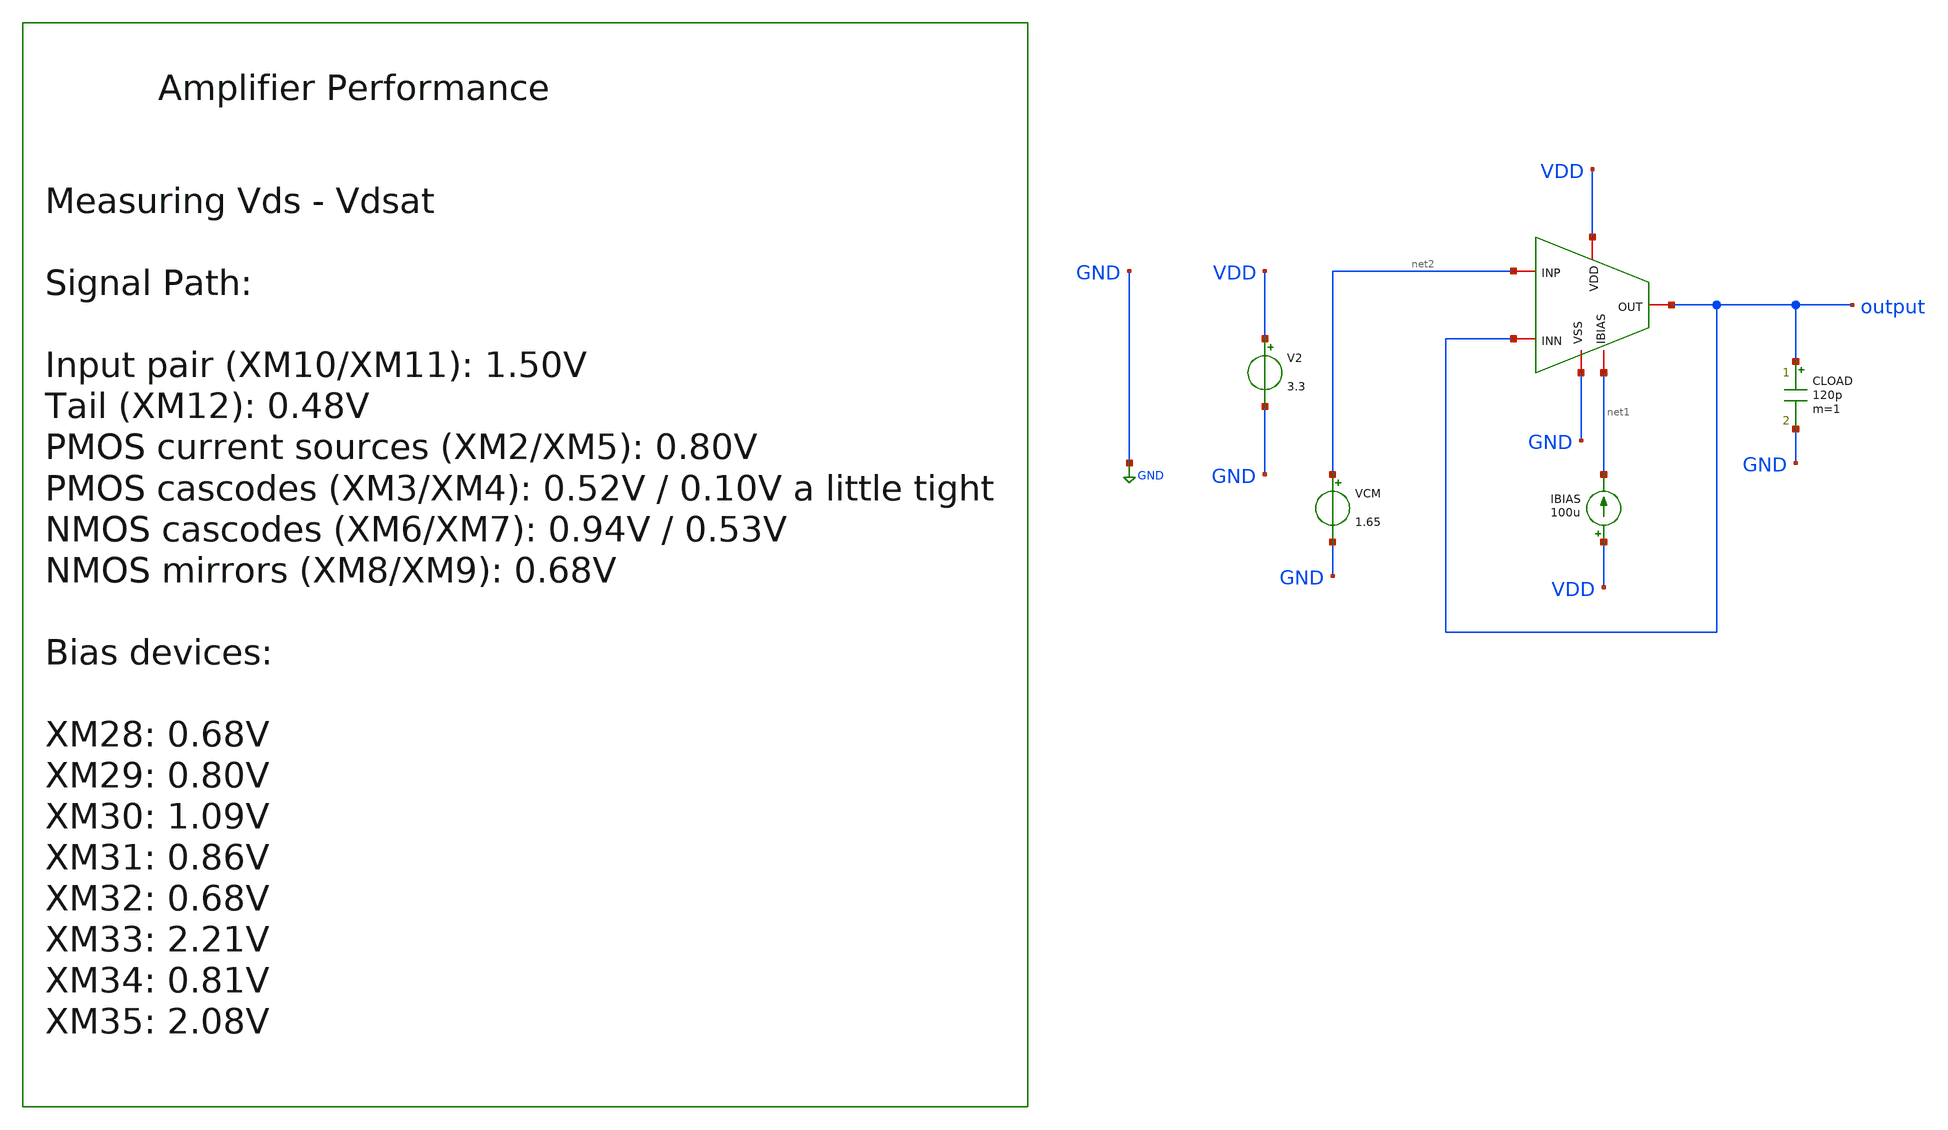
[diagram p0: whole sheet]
** sch_path: designs/libs/core_amps/ota_folded_cascode_new/tb/op_vds_tb.sch
**.subckt op_vds_tb
IBIAS VDD net1 100u
V2 VDD GND 3.3
CLOAD output GND 120p m=1
VCM net2 GND 1.65
x1 VDD GND output net2 output net1 ota_folded_cascode
**** begin user architecture code

.include $::180MCU_MODELS/design.ngspice
.lib $::180MCU_MODELS/sm141064.ngspice typical



.control
op

let sat_xm28 = abs(@m.x1.xm28.m0[vds]) - abs(@m.x1.xm28.m0[vdsat])
let sat_xm33 = abs(@m.x1.xm33.m0[vds]) - abs(@m.x1.xm33.m0[vdsat])
let sat_xm32 = abs(@m.x1.xm32.m0[vds]) - abs(@m.x1.xm32.m0[vdsat])
let sat_xm29 = abs(@m.x1.xm29.m0[vds]) - abs(@m.x1.xm29.m0[vdsat])
let sat_xm30 = abs(@m.x1.xm30.m0[vds]) - abs(@m.x1.xm30.m0[vdsat])
let sat_xm31 = abs(@m.x1.xm31.m0[vds]) - abs(@m.x1.xm31.m0[vdsat])
let sat_xm34 = abs(@m.x1.xm34.m0[vds]) - abs(@m.x1.xm34.m0[vdsat])
let sat_xm35 = abs(@m.x1.xm35.m0[vds]) - abs(@m.x1.xm35.m0[vdsat])
let sat_xm11 = abs(@m.x1.xm11.m0[vds]) - abs(@m.x1.xm11.m0[vdsat])
let sat_xm10 = abs(@m.x1.xm10.m0[vds]) - abs(@m.x1.xm10.m0[vdsat])
let sat_xm12 = abs(@m.x1.xm12.m0[vds]) - abs(@m.x1.xm12.m0[vdsat])
let sat_xm2  = abs(@m.x1.xm2.m0[vds]) - abs(@m.x1.xm2.m0[vdsat])
let sat_xm3  = abs(@m.x1.xm3.m0[vds]) - abs(@m.x1.xm3.m0[vdsat])
let sat_xm4  = abs(@m.x1.xm4.m0[vds]) - abs(@m.x1.xm4.m0[vdsat])
let sat_xm5  = abs(@m.x1.xm5.m0[vds]) - abs(@m.x1.xm5.m0[vdsat])
let sat_xm6  = abs(@m.x1.xm6.m0[vds]) - abs(@m.x1.xm6.m0[vdsat])
let sat_xm7  = abs(@m.x1.xm7.m0[vds]) - abs(@m.x1.xm7.m0[vdsat])
let sat_xm8  = abs(@m.x1.xm8.m0[vds]) - abs(@m.x1.xm8.m0[vdsat])
let sat_xm9  = abs(@m.x1.xm9.m0[vds]) - abs(@m.x1.xm9.m0[vdsat])
print sat_xm28 sat_xm33 sat_xm32 sat_xm29
print sat_xm30 sat_xm31 sat_xm34 sat_xm35
print sat_xm11 sat_xm10 sat_xm12
print sat_xm2 sat_xm3 sat_xm4 sat_xm5
print sat_xm6 sat_xm7 sat_xm8 sat_xm9

.endc


**** end user architecture code
**.ends
.GLOBAL GND
.end
